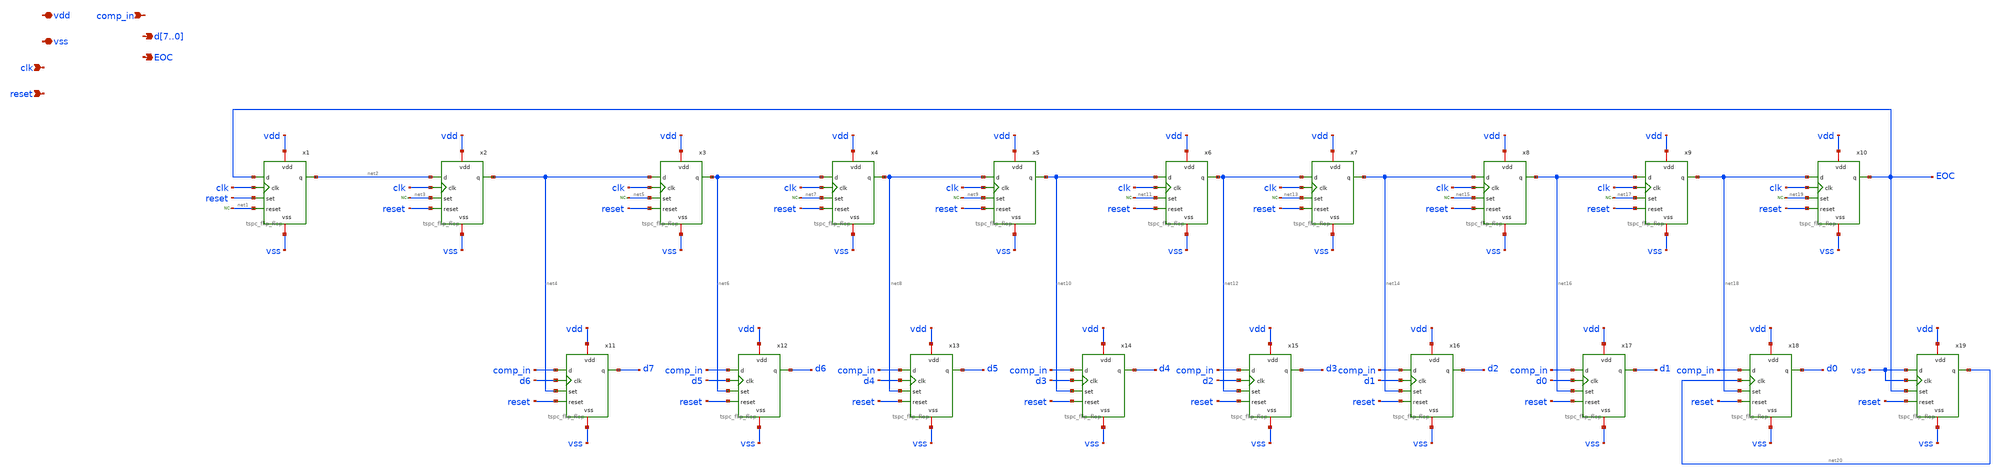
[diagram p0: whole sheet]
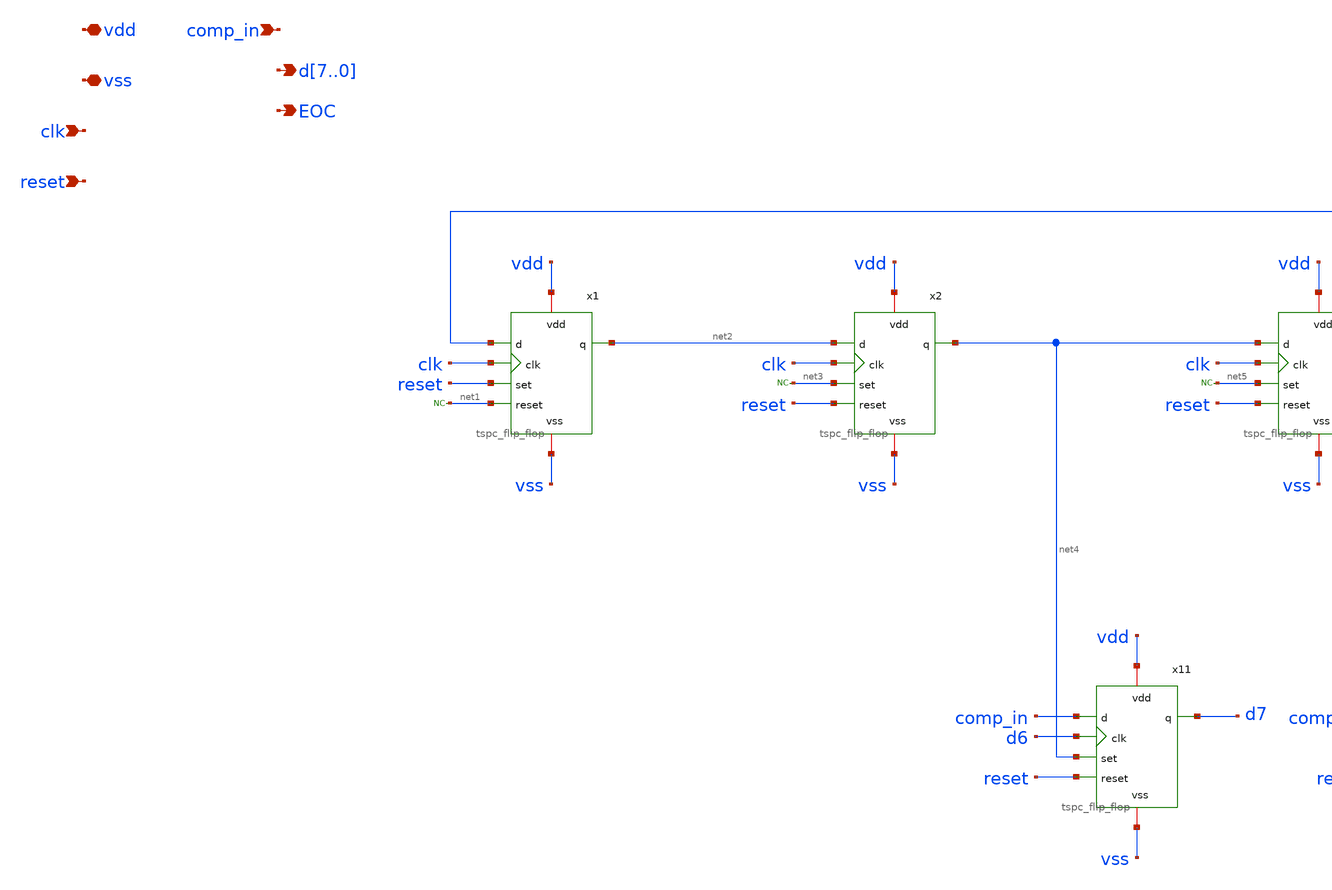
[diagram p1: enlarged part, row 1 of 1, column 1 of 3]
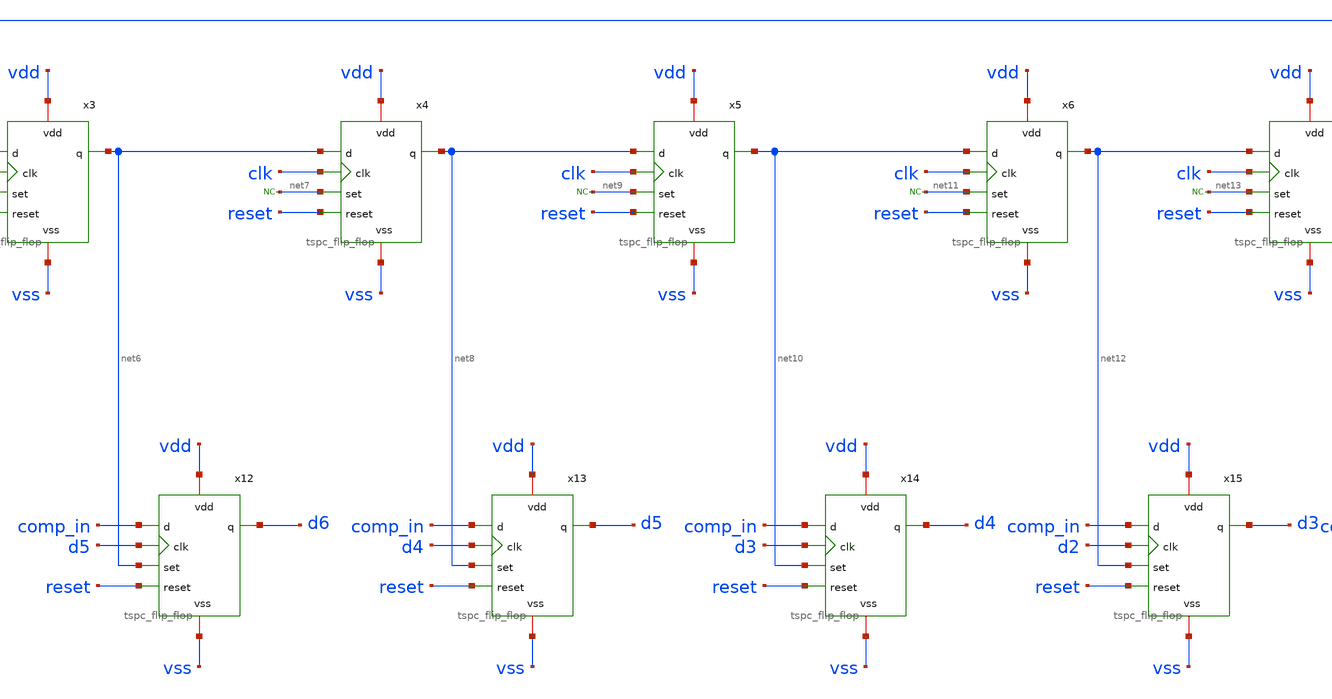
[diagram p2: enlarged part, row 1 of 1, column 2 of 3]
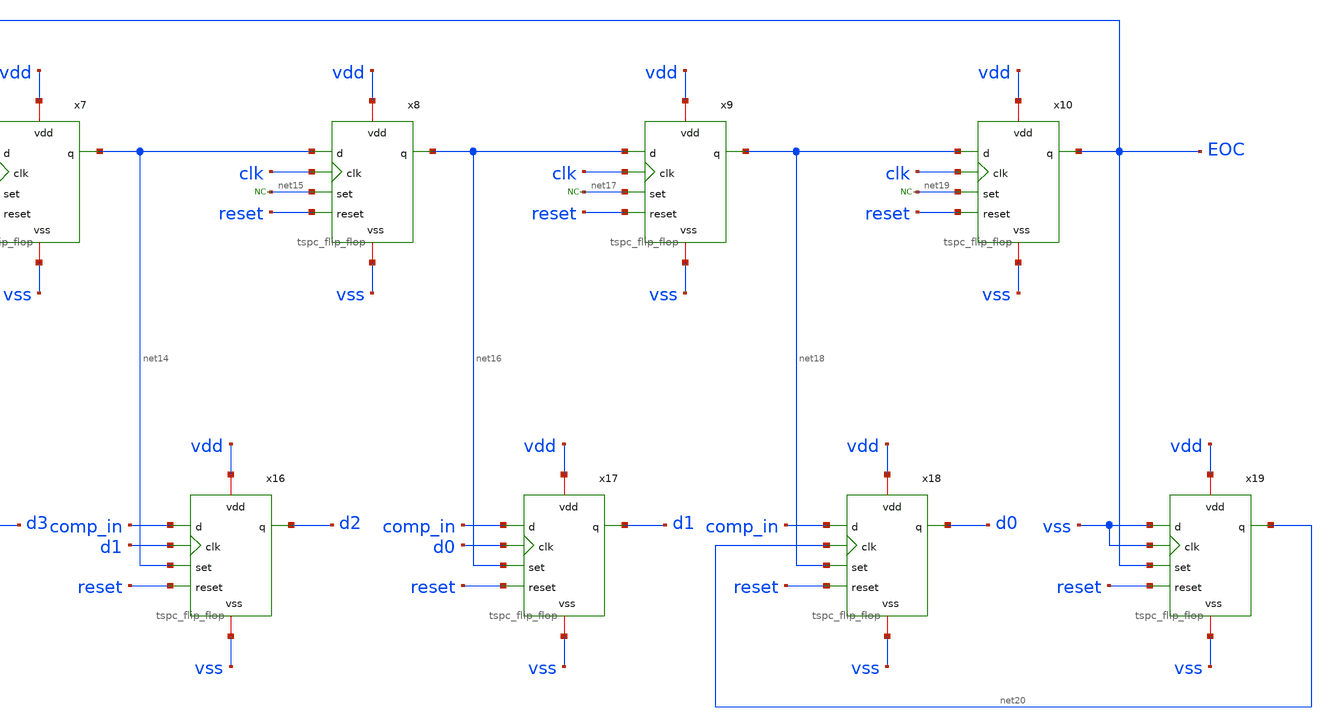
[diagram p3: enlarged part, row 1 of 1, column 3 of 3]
** sch_path: designs/libs/SAR_logic/SAR_logic.sch
**.subckt SAR_logic comp_in vdd vss clk reset d7,d6,d5,d4,d3,d2,d1,d0 EOC
*.ipin comp_in
*.iopin vdd
*.iopin vss
*.ipin clk
*.ipin reset
*.opin d7,d6,d5,d4,d3,d2,d1,d0
*.opin EOC
x1 vdd vss EOC clk reset net1 net2 tspc_flip_flop
* noconn #net1
x2 vdd vss net2 clk net3 reset net4 tspc_flip_flop
* noconn #net3
x3 vdd vss net4 clk net5 reset net6 tspc_flip_flop
* noconn #net5
x4 vdd vss net6 clk net7 reset net8 tspc_flip_flop
* noconn #net7
x5 vdd vss net8 clk net9 reset net10 tspc_flip_flop
* noconn #net9
x6 vdd vss net10 clk net11 reset net12 tspc_flip_flop
* noconn #net11
x7 vdd vss net12 clk net13 reset net14 tspc_flip_flop
* noconn #net13
x8 vdd vss net14 clk net15 reset net16 tspc_flip_flop
* noconn #net15
x9 vdd vss net16 clk net17 reset net18 tspc_flip_flop
* noconn #net17
x10 vdd vss net18 clk net19 reset EOC tspc_flip_flop
* noconn #net19
x11 vdd vss comp_in d6 net4 reset d7 tspc_flip_flop
x12 vdd vss comp_in d5 net6 reset d6 tspc_flip_flop
x13 vdd vss comp_in d4 net8 reset d5 tspc_flip_flop
x14 vdd vss comp_in d3 net10 reset d4 tspc_flip_flop
x15 vdd vss comp_in d2 net12 reset d3 tspc_flip_flop
x16 vdd vss comp_in d1 net14 reset d2 tspc_flip_flop
x17 vdd vss comp_in d0 net16 reset d1 tspc_flip_flop
x18 vdd vss comp_in net20 net18 reset d0 tspc_flip_flop
x19 vdd vss vss vss EOC reset net20 tspc_flip_flop
**.ends

* expanding   symbol:  libs/tspc_flip_flop/tspc_flip_flop.sym # of pins=7
** sym_path: designs/libs/tspc_flip_flop/tspc_flip_flop.sym
** sch_path: designs/libs/tspc_flip_flop/tspc_flip_flop.sch
.subckt tspc_flip_flop vdd vss d clk set reset q
*.iopin vdd
*.iopin vss
*.ipin d
*.ipin clk
*.ipin set
*.ipin reset
*.opin q
XM1 b1 d vss vss nfet_03v3 L=0.28u W=1u nf=1 ad='int((nf+1)/2) * W/nf * 0.18u' as='int((nf+2)/2) * W/nf * 0.18u'
+ pd='2*int((nf+1)/2) * (W/nf + 0.18u)' ps='2*int((nf+2)/2) * (W/nf + 0.18u)' nrd='0.18u / W' nrs='0.18u / W'
+ sa=0 sb=0 sd=0 m=1
XM2 b1 clk net1 net1 pfet_03v3 L=0.28u W=2u nf=1 ad='int((nf+1)/2) * W/nf * 0.18u' as='int((nf+2)/2) * W/nf * 0.18u'
+ pd='2*int((nf+1)/2) * (W/nf + 0.18u)' ps='2*int((nf+2)/2) * (W/nf + 0.18u)' nrd='0.18u / W' nrs='0.18u / W'
+ sa=0 sb=0 sd=0 m=1
XM3 net1 d vdd vdd pfet_03v3 L=0.28u W=2u nf=1 ad='int((nf+1)/2) * W/nf * 0.18u' as='int((nf+2)/2) * W/nf * 0.18u'
+ pd='2*int((nf+1)/2) * (W/nf + 0.18u)' ps='2*int((nf+2)/2) * (W/nf + 0.18u)' nrd='0.18u / W' nrs='0.18u / W'
+ sa=0 sb=0 sd=0 m=1
XM4 b2 clk vdd vdd pfet_03v3 L=0.28u W=2u nf=1 ad='int((nf+1)/2) * W/nf * 0.18u' as='int((nf+2)/2) * W/nf * 0.18u'
+ pd='2*int((nf+1)/2) * (W/nf + 0.18u)' ps='2*int((nf+2)/2) * (W/nf + 0.18u)' nrd='0.18u / W' nrs='0.18u / W'
+ sa=0 sb=0 sd=0 m=1
XM5 b2 b1 net2 vss nfet_03v3 L=0.28u W=1u nf=1 ad='int((nf+1)/2) * W/nf * 0.18u' as='int((nf+2)/2) * W/nf * 0.18u'
+ pd='2*int((nf+1)/2) * (W/nf + 0.18u)' ps='2*int((nf+2)/2) * (W/nf + 0.18u)' nrd='0.18u / W' nrs='0.18u / W'
+ sa=0 sb=0 sd=0 m=1
XM6 net2 clk vss vss nfet_03v3 L=0.28u W=1u nf=1 ad='int((nf+1)/2) * W/nf * 0.18u' as='int((nf+2)/2) * W/nf * 0.18u'
+ pd='2*int((nf+1)/2) * (W/nf + 0.18u)' ps='2*int((nf+2)/2) * (W/nf + 0.18u)' nrd='0.18u / W' nrs='0.18u / W'
+ sa=0 sb=0 sd=0 m=1
XM7 net4 b2 vss vss nfet_03v3 L=0.28u W=1u nf=1 ad='int((nf+1)/2) * W/nf * 0.18u' as='int((nf+2)/2) * W/nf * 0.18u'
+ pd='2*int((nf+1)/2) * (W/nf + 0.18u)' ps='2*int((nf+2)/2) * (W/nf + 0.18u)' nrd='0.18u / W' nrs='0.18u / W'
+ sa=0 sb=0 sd=0 m=1
XM8 b3 clk net4 vss nfet_03v3 L=0.28u W=1u nf=1 ad='int((nf+1)/2) * W/nf * 0.18u' as='int((nf+2)/2) * W/nf * 0.18u'
+ pd='2*int((nf+1)/2) * (W/nf + 0.18u)' ps='2*int((nf+2)/2) * (W/nf + 0.18u)' nrd='0.18u / W' nrs='0.18u / W'
+ sa=0 sb=0 sd=0 m=1
XM9 b3 set net3 net3 pfet_03v3 L=0.28u W=2u nf=1 ad='int((nf+1)/2) * W/nf * 0.18u' as='int((nf+2)/2) * W/nf * 0.18u'
+ pd='2*int((nf+1)/2) * (W/nf + 0.18u)' ps='2*int((nf+2)/2) * (W/nf + 0.18u)' nrd='0.18u / W' nrs='0.18u / W'
+ sa=0 sb=0 sd=0 m=1
XM10 net3 b2 vdd vdd pfet_03v3 L=0.28u W=2u nf=1 ad='int((nf+1)/2) * W/nf * 0.18u' as='int((nf+2)/2) * W/nf * 0.18u'
+ pd='2*int((nf+1)/2) * (W/nf + 0.18u)' ps='2*int((nf+2)/2) * (W/nf + 0.18u)' nrd='0.18u / W' nrs='0.18u / W'
+ sa=0 sb=0 sd=0 m=1
XM11 b3 net5 vdd vdd pfet_03v3 L=0.28u W=2u nf=1 ad='int((nf+1)/2) * W/nf * 0.18u' as='int((nf+2)/2) * W/nf * 0.18u'
+ pd='2*int((nf+1)/2) * (W/nf + 0.18u)' ps='2*int((nf+2)/2) * (W/nf + 0.18u)' nrd='0.18u / W' nrs='0.18u / W'
+ sa=0 sb=0 sd=0 m=1
XM12 b3 set vss vss nfet_03v3 L=0.28u W=1u nf=1 ad='int((nf+1)/2) * W/nf * 0.18u' as='int((nf+2)/2) * W/nf * 0.18u'
+ pd='2*int((nf+1)/2) * (W/nf + 0.18u)' ps='2*int((nf+2)/2) * (W/nf + 0.18u)' nrd='0.18u / W' nrs='0.18u / W'
+ sa=0 sb=0 sd=0 m=1
XM13 q b3 vdd vdd pfet_03v3 L=0.28u W=2u nf=1 ad='int((nf+1)/2) * W/nf * 0.18u' as='int((nf+2)/2) * W/nf * 0.18u'
+ pd='2*int((nf+1)/2) * (W/nf + 0.18u)' ps='2*int((nf+2)/2) * (W/nf + 0.18u)' nrd='0.18u / W' nrs='0.18u / W'
+ sa=0 sb=0 sd=0 m=1
XM14 q b3 vss vss nfet_03v3 L=0.28u W=1u nf=1 ad='int((nf+1)/2) * W/nf * 0.18u' as='int((nf+2)/2) * W/nf * 0.18u'
+ pd='2*int((nf+1)/2) * (W/nf + 0.18u)' ps='2*int((nf+2)/2) * (W/nf + 0.18u)' nrd='0.18u / W' nrs='0.18u / W'
+ sa=0 sb=0 sd=0 m=1
XM15 net5 reset vdd vdd pfet_03v3 L=0.28u W=2u nf=1 ad='int((nf+1)/2) * W/nf * 0.18u' as='int((nf+2)/2) * W/nf * 0.18u'
+ pd='2*int((nf+1)/2) * (W/nf + 0.18u)' ps='2*int((nf+2)/2) * (W/nf + 0.18u)' nrd='0.18u / W' nrs='0.18u / W'
+ sa=0 sb=0 sd=0 m=1
XM16 net5 reset vss vss nfet_03v3 L=0.28u W=1u nf=1 ad='int((nf+1)/2) * W/nf * 0.18u' as='int((nf+2)/2) * W/nf * 0.18u'
+ pd='2*int((nf+1)/2) * (W/nf + 0.18u)' ps='2*int((nf+2)/2) * (W/nf + 0.18u)' nrd='0.18u / W' nrs='0.18u / W'
+ sa=0 sb=0 sd=0 m=1
.ends

.end
